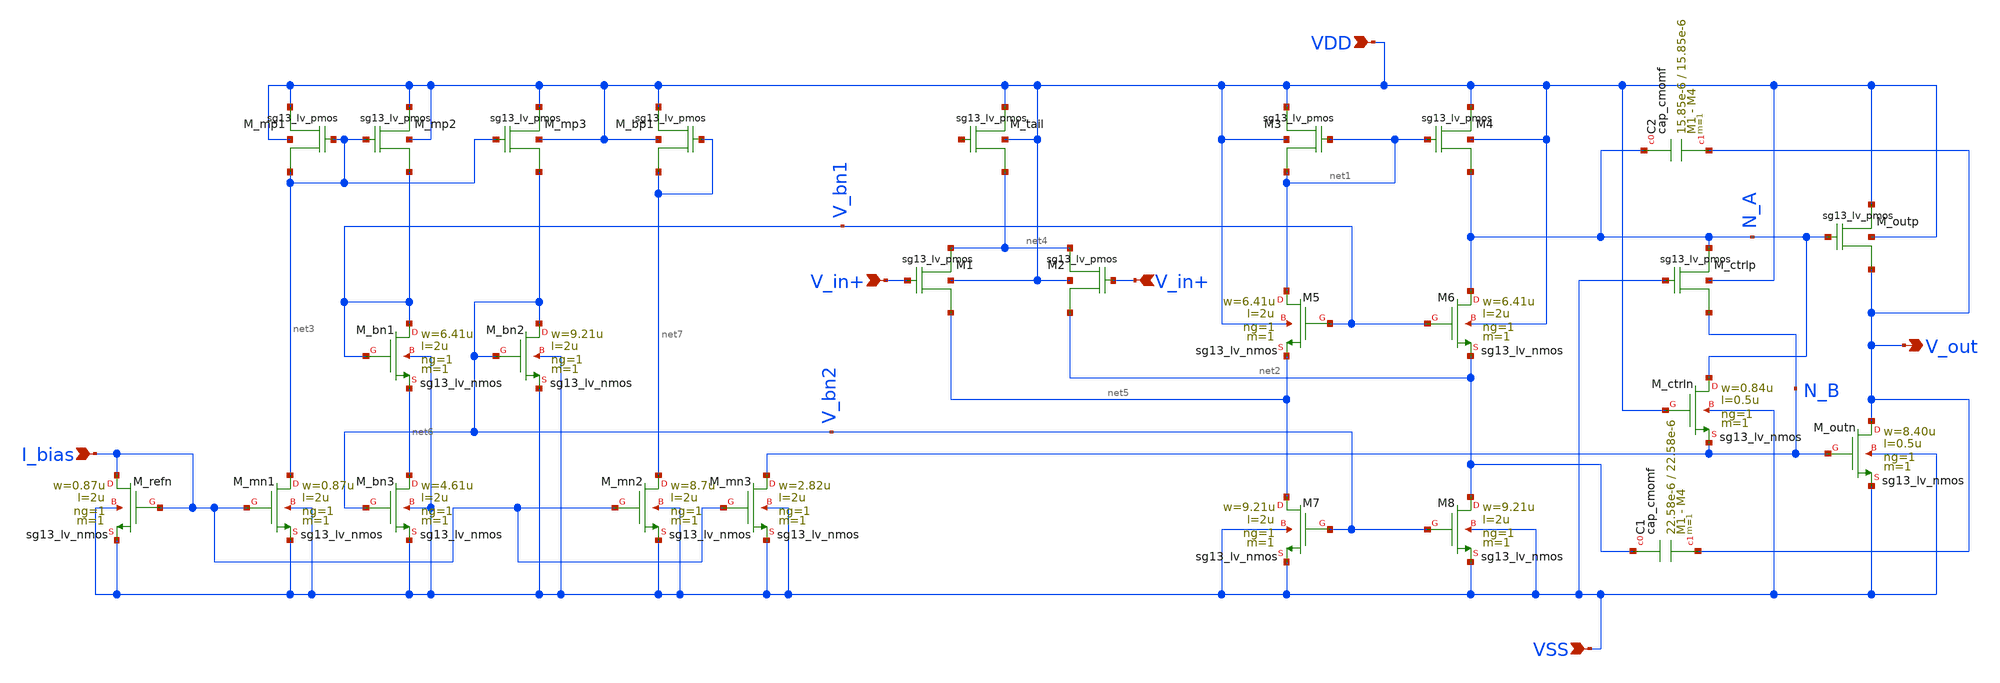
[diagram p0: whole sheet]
** sch_path: designs/libs/core_analog/coarse_gain/cg-ota.sch
**.subckt cg-ota V_in+ VDD VSS V_out I_bias V_in+
*.ipin V_in+
*.ipin VDD
*.ipin VSS
*.opin V_out
*.ipin I_bias
*.ipin V_in+
XM1 net4 V_in+ net5 VDD sg13_lv_pmos w=26.56u l=2u ng=4 m=1
XM2 net4 V_in+ net2 VDD sg13_lv_pmos w=26.56u l=2u ng=4 m=1
XM3 VDD net1 net1 VDD sg13_lv_pmos w=7.33u l=2u ng=1 m=1
XM4 VDD net1 N_A VDD sg13_lv_pmos w=7.33u l=2u ng=1 m=1
XM7 net5 V_bn2 VSS VSS sg13_lv_nmos w=9.21u l=2u ng=1 m=1 mm_ok=1
XM8 net2 V_bn2 VSS VSS sg13_lv_nmos w=9.21u l=2u ng=1 m=1 mm_ok=1
XM_tail VDD net8 net4 VDD sg13_lv_pmos w=5.33u l=2u ng=1 m=4
XM_ctrlp N_A VSS N_B VDD sg13_lv_pmos w=2.20u l=0.50u ng=1 m=1
XM_outp VDD N_A V_out VDD sg13_lv_pmos w=22.20u l=0.5u ng=4 m=1
XM_ctrln N_A VDD N_B VSS sg13_lv_nmos w=0.84u l=0.5u ng=1 m=1 mm_ok=1
XM_outn V_out N_B VSS VSS sg13_lv_nmos w=8.40u l=0.5u ng=1 m=1 mm_ok=1
XC1 net2 V_out cap_cmomf w=22.58e-6 l=22.58e-6 mmin=1 mmax=4 subblock=0 rfmodel=0 subscale=1 m=1
+ mm_ok=1
XC2 N_A V_out cap_cmomf w=15.85e-6 l=15.85e-6 mmin=1 mmax=4 subblock=0 rfmodel=0 subscale=1 m=1
+ mm_ok=1
XM5 net1 V_bn1 net5 VDD sg13_lv_nmos w=6.41u l=2u ng=1 m=1 mm_ok=1
XM6 N_A V_bn1 net2 VDD sg13_lv_nmos w=6.41u l=2u ng=1 m=1 mm_ok=1
XM_mp1 VDD net3 net3 VDD sg13_lv_pmos w=2.30u l=2u ng=1 m=1
XM_mn1 net3 I_bias VSS VSS sg13_lv_nmos w=0.87u l=2u ng=1 m=1 mm_ok=1
XM_refn I_bias I_bias VSS VSS sg13_lv_nmos w=0.87u l=2u ng=1 m=1 mm_ok=1
XM_mp2 VDD net3 V_bn1 VDD sg13_lv_pmos w=11.50u l=2u ng=2 m=1
XM_mp3 VDD net3 V_bn2 VDD sg13_lv_pmos w=22.30u l=2u ng=4 m=1
XM_bn1 V_bn1 V_bn1 net6 VSS sg13_lv_nmos w=6.41u l=2u ng=1 m=1 mm_ok=1
XM_bn2 V_bn2 V_bn2 VSS VSS sg13_lv_nmos w=9.21u l=2u ng=1 m=1 mm_ok=1
XM_bn3 net6 V_bn2 VSS VSS sg13_lv_nmos w=4.61u l=2u ng=1 m=1 mm_ok=1
XM_mn2 net7 I_bias VSS VSS sg13_lv_nmos w=8.7u l=2u ng=1 m=1 mm_ok=1
XM_bp1 VDD net7 net7 VDD sg13_lv_pmos w=5.33u l=2u ng=1 m=4
XM_mn3 N_B I_bias VSS VSS sg13_lv_nmos w=2.82u l=2u ng=1 m=1 mm_ok=1
**.ends
.end
